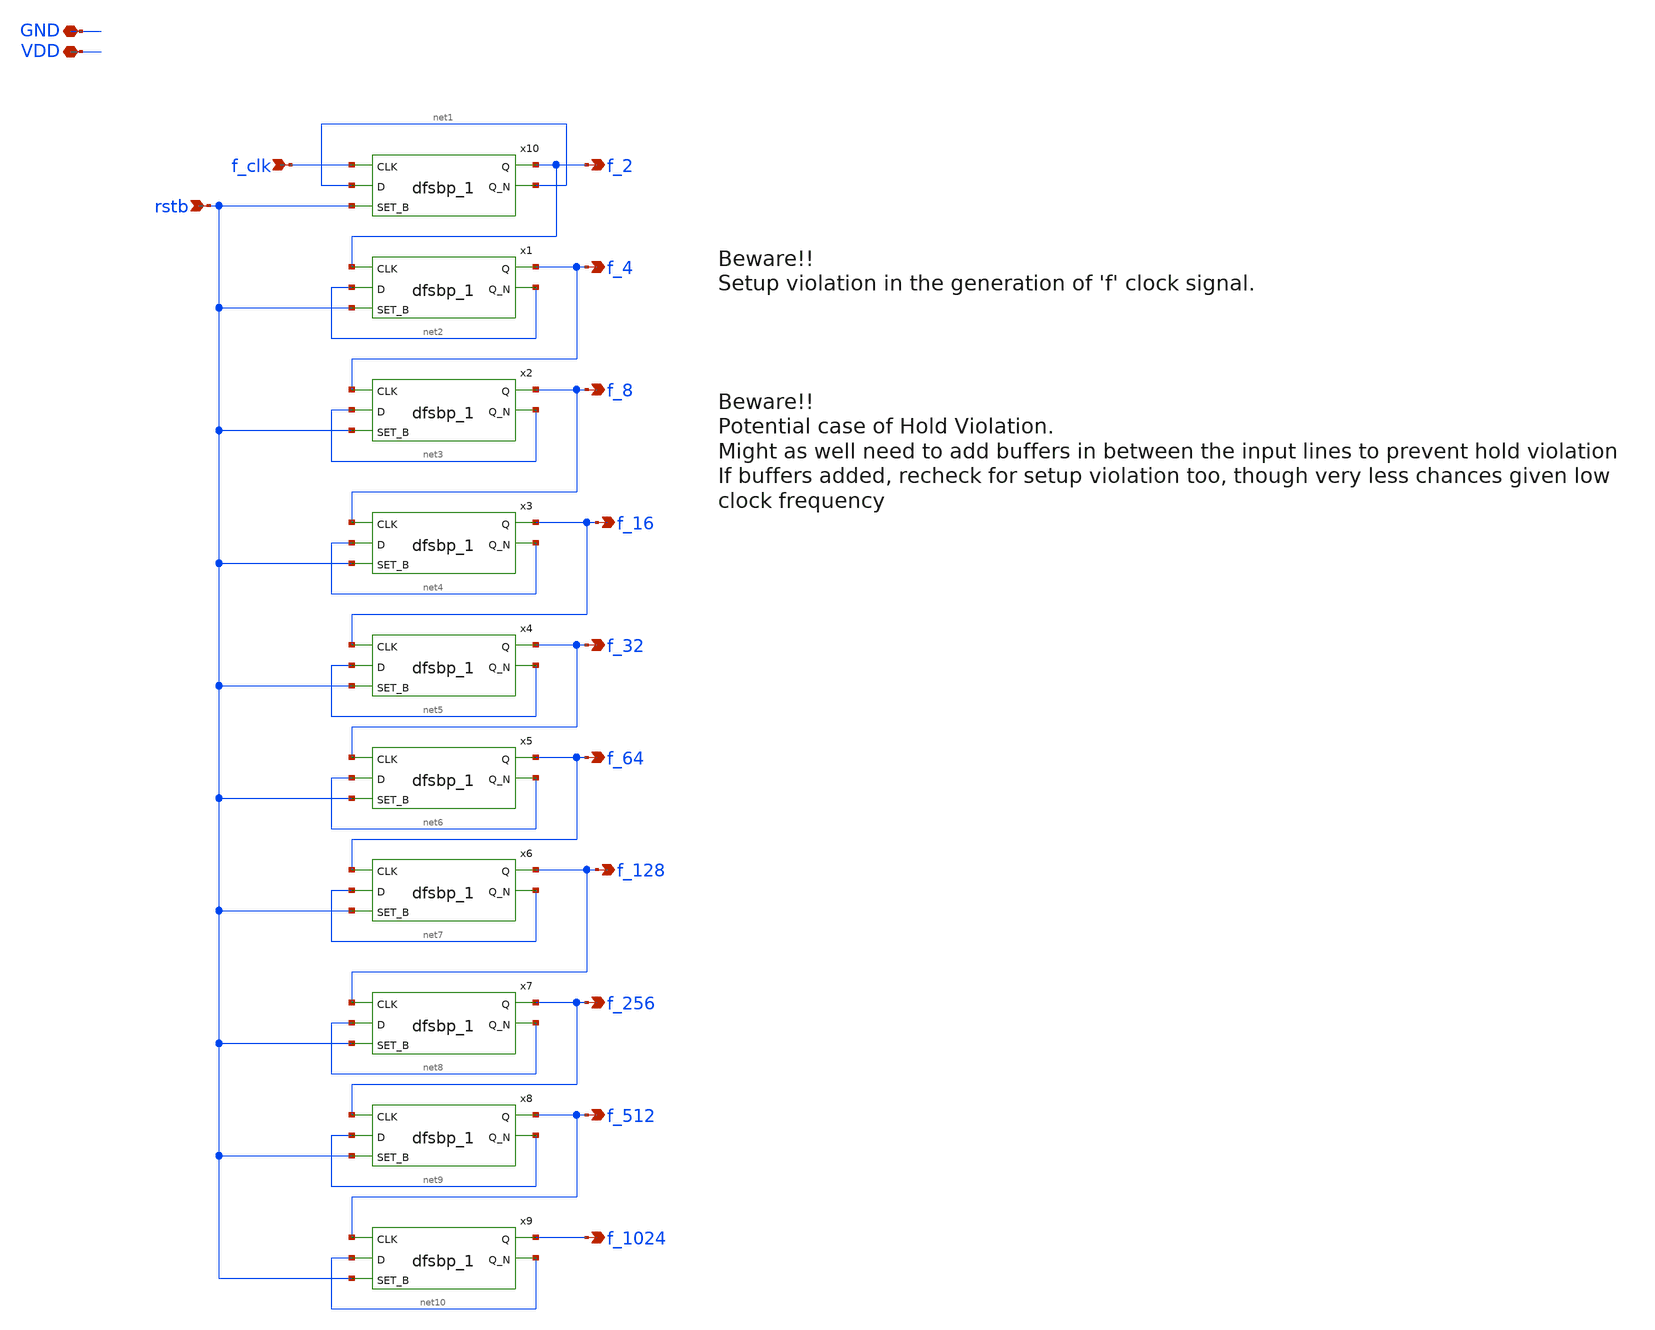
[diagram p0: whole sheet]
** sch_path: xschem/gray selector/clk_tree_fb.sch
**.subckt clk_tree_fb rstb VDD GND f_2 f_4 f_8 f_16 f_32 f_64 f_128 f_256 f_512 f_clk f_1024
*.ipin rstb
*.iopin VDD
*.iopin GND
*.opin f_2
*.opin f_4
*.opin f_8
*.opin f_16
*.opin f_32
*.opin f_64
*.opin f_128
*.opin f_256
*.opin f_512
*.ipin f_clk
*.opin f_1024
x10 f_clk net1 rstb GND GND VDD VDD f_2 net1 sky130_fd_sc_lp__dfsbp_1
x1 f_2 net2 rstb GND GND VDD VDD f_4 net2 sky130_fd_sc_lp__dfsbp_1
x2 f_4 net3 rstb GND GND VDD VDD f_8 net3 sky130_fd_sc_lp__dfsbp_1
x3 f_8 net4 rstb GND GND VDD VDD f_16 net4 sky130_fd_sc_lp__dfsbp_1
x4 f_16 net5 rstb GND GND VDD VDD f_32 net5 sky130_fd_sc_lp__dfsbp_1
x5 f_32 net6 rstb GND GND VDD VDD f_64 net6 sky130_fd_sc_lp__dfsbp_1
x6 f_64 net7 rstb GND GND VDD VDD f_128 net7 sky130_fd_sc_lp__dfsbp_1
x7 f_128 net8 rstb GND GND VDD VDD f_256 net8 sky130_fd_sc_lp__dfsbp_1
x8 f_256 net9 rstb GND GND VDD VDD f_512 net9 sky130_fd_sc_lp__dfsbp_1
x9 f_512 net10 rstb GND GND VDD VDD f_1024 net10 sky130_fd_sc_lp__dfsbp_1
**.ends
.end
